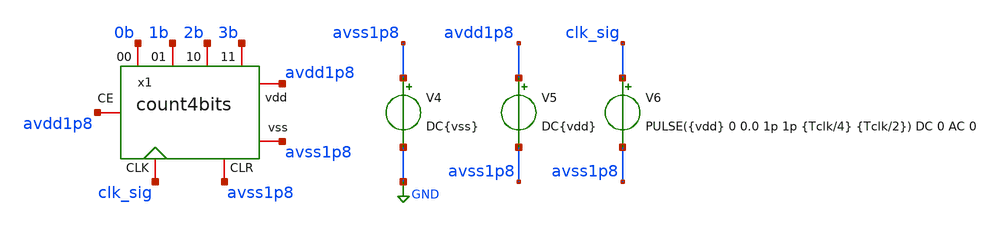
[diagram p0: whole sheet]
** sch_path: verification/testbenches/count4bits/tb_count4bits.sch
**.subckt tb_count4bits
x1 avdd1p8 avss1p8 avdd1p8 0b clk_sig avss1p8 1b 2b 3b count4bits
V4 avss1p8 GND DC{vss}
V5 avdd1p8 avss1p8 DC{vdd}
V6 clk_sig avss1p8 PULSE({vdd} 0 0.0 1p 1p {Tclk/4} {Tclk/2}) DC 0 AC 0
**** begin user architecture code


* Circuit Parameters
.param vdd = 1.8
.param vss = 0.0
.param Tclk = 10n
.options TEMP = 65.0
* Include Models
.lib /foss/pdks/sky130A/libs.tech/ngspice/sky130.lib.spice TT
* OP Parameters & Singals to save
.save all
*Simulations
.control
tran 0.01u 100n
setplot tran1
plot v(clk_sig) v(0b)+2 v(1b)+4 v(2b)+6 v(3b)+8
reset
dc V6 0 1.8 0.01
setplot dc
set filetype = ascii
write dcsweep.raw
.endc
.end


**** end user architecture code
**.ends
.GLOBAL GND
.end
